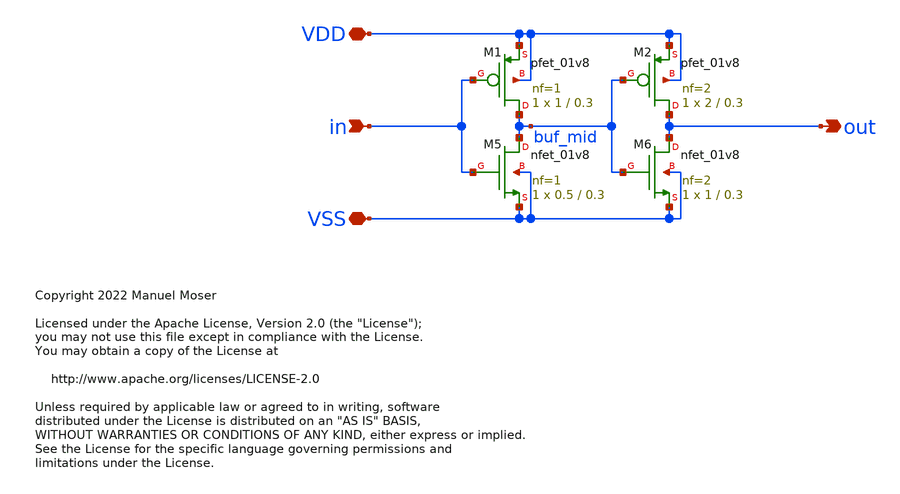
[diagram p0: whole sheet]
** sch_path: Circuits/Comparator/adc_comp_buffer.sch
* Copyright 2022 Manuel Moser
* Licensed under the Apache License, Version 2.0 (the "License");
**.subckt adc_comp_buffer VDD VSS in out
*.iopin VDD
*.iopin VSS
*.ipin in
*.opin out
XM5 buf_mid in VSS VSS sky130_fd_pr__nfet_01v8 L=0.3 W=0.5 nf=1 ad='int((nf+1)/2) * W/nf * 0.29' as='int((nf+2)/2) * W/nf * 0.29'
+ pd='2*int((nf+1)/2) * (W/nf + 0.29)' ps='2*int((nf+2)/2) * (W/nf + 0.29)' nrd='0.29 / W' nrs='0.29 / W'
+ sa=0 sb=0 sd=0 mult=1 m=1
XM1 buf_mid in VDD VDD sky130_fd_pr__pfet_01v8 L=0.3 W=1 nf=1 ad='int((nf+1)/2) * W/nf * 0.29' as='int((nf+2)/2) * W/nf * 0.29'
+ pd='2*int((nf+1)/2) * (W/nf + 0.29)' ps='2*int((nf+2)/2) * (W/nf + 0.29)' nrd='0.29 / W' nrs='0.29 / W'
+ sa=0 sb=0 sd=0 mult=1 m=1
XM2 out buf_mid VDD VDD sky130_fd_pr__pfet_01v8 L=0.3 W=2 nf=2 ad='int((nf+1)/2) * W/nf * 0.29' as='int((nf+2)/2) * W/nf * 0.29'
+ pd='2*int((nf+1)/2) * (W/nf + 0.29)' ps='2*int((nf+2)/2) * (W/nf + 0.29)' nrd='0.29 / W' nrs='0.29 / W'
+ sa=0 sb=0 sd=0 mult=1 m=1
XM6 out buf_mid VSS VSS sky130_fd_pr__nfet_01v8 L=0.3 W=1 nf=2 ad='int((nf+1)/2) * W/nf * 0.29' as='int((nf+2)/2) * W/nf * 0.29'
+ pd='2*int((nf+1)/2) * (W/nf + 0.29)' ps='2*int((nf+2)/2) * (W/nf + 0.29)' nrd='0.29 / W' nrs='0.29 / W'
+ sa=0 sb=0 sd=0 mult=1 m=1
**.ends
.end
